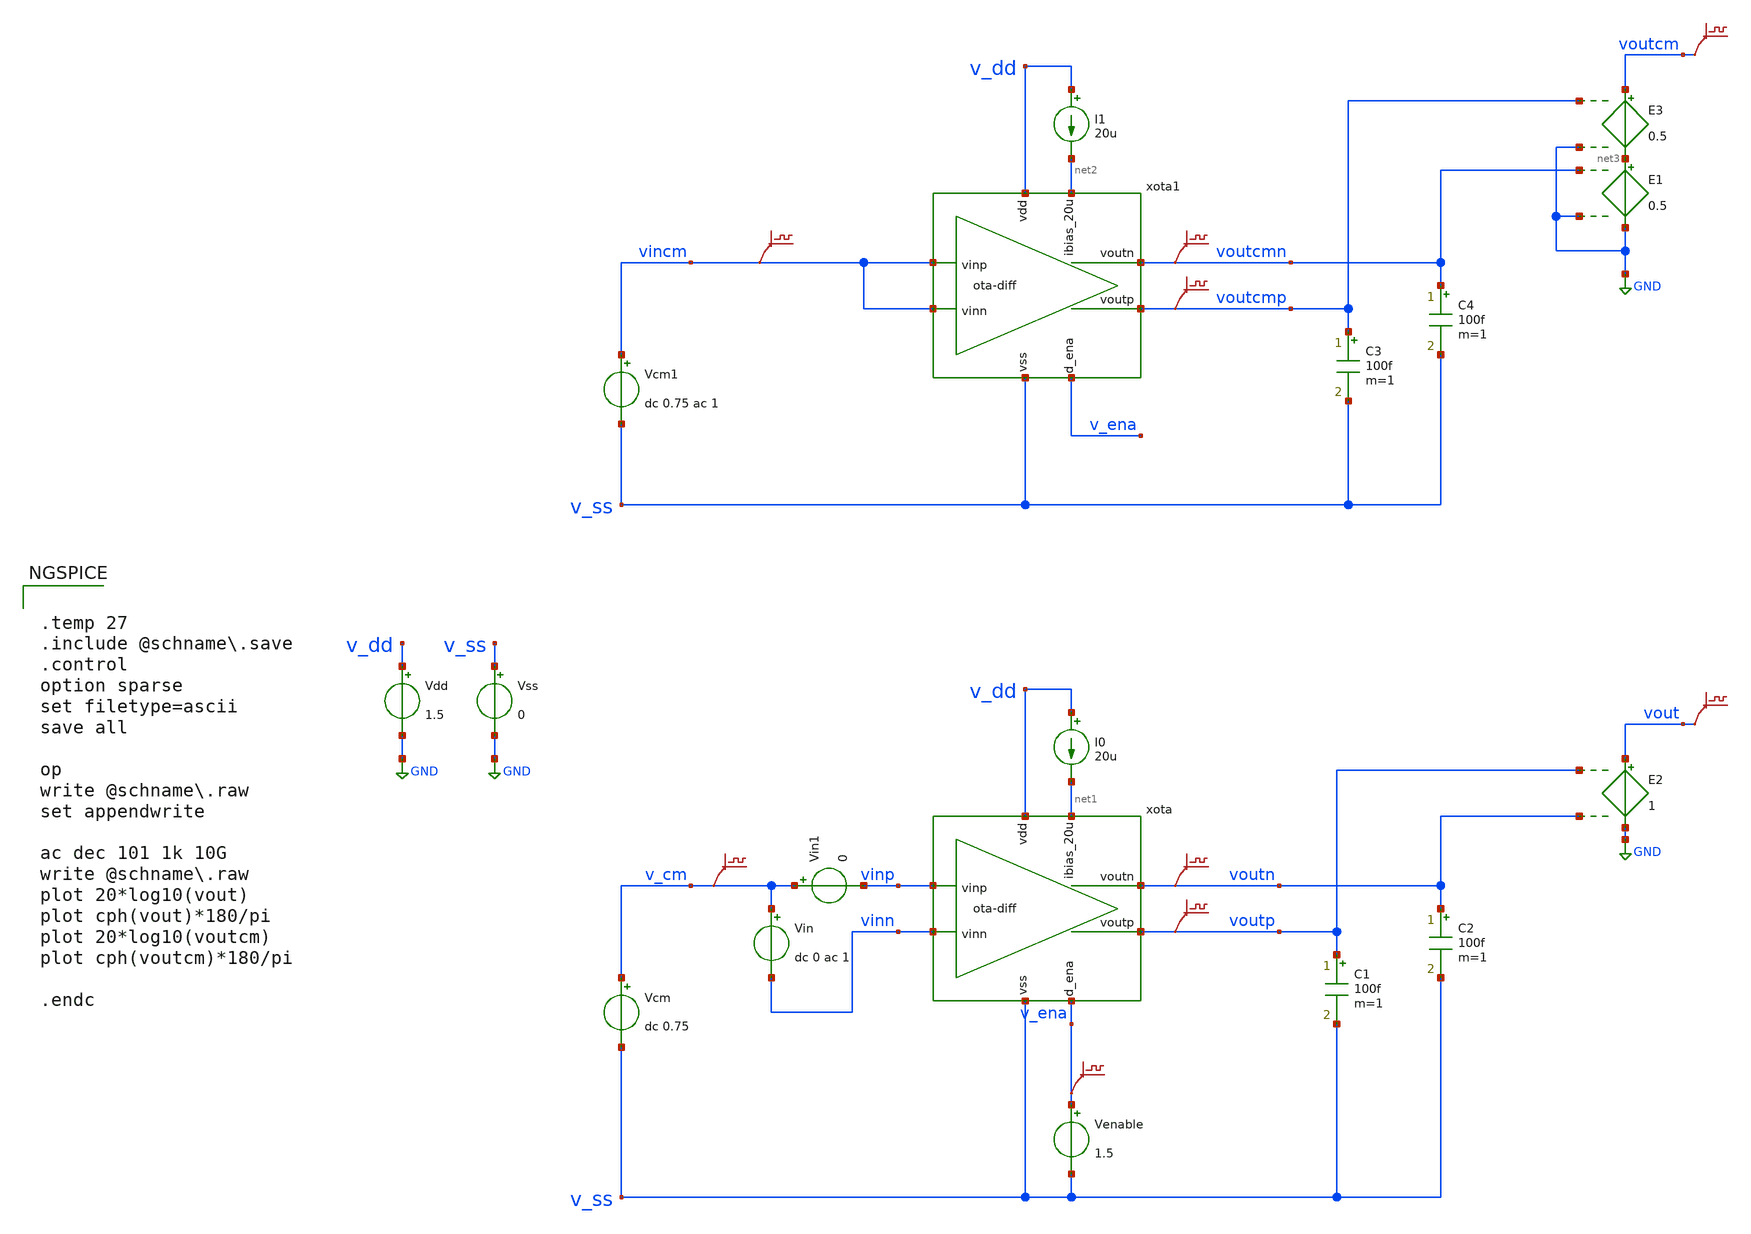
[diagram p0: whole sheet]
** sch_path: xschem/ota-diff_tb-acol.sch
* (c) 2024-2025 Harald Pretl, Apache-2.0 license
**.subckt ota-diff_tb-acol
Vdd v_dd GND 1.5
xota v_dd vinp vinn net1 v_ena v_ss voutn voutp ota-diff
Vss v_ss GND 0
C1 voutp v_ss 100f m=1
Vcm v_cm v_ss dc 0.75
I0 v_dd net1 20u
Venable v_ena v_ss 1.5
.save v(v_cm)
.save v(voutp)
.save v(v_ena)
Vin v_cm vinn dc 0 ac 1
C2 voutn v_ss 100f m=1
.save v(voutn)
xota1 v_dd vincm vincm net2 v_ena v_ss voutcmn voutcmp ota-diff
C3 voutcmp v_ss 100f m=1
Vcm1 vincm v_ss dc 0.75 ac 1
I1 v_dd net2 20u
.save v(vincm)
.save v(voutcmp)
C4 voutcmn v_ss 100f m=1
.save v(voutcmn)
E1 net3 GND voutcmn GND 0.5
.save v(voutcm)
E2 vout GND voutp voutn 1
.save v(vout)
E3 voutcm net3 voutcmp GND 0.5
Vin1 v_cm vinp 0
**** begin user architecture code

.lib cornerMOSlv.lib mos_tt
.lib cornerRES.lib res_typ
.lib cornerCAP.lib cap_typ



.temp 27
.include @schname\.save
.control
option sparse
set filetype=ascii
save all

op
write @schname\.raw
set appendwrite

ac dec 101 1k 10G
write @schname\.raw
plot 20*log10(vout)
plot cph(vout)*180/pi
plot 20*log10(voutcm)
plot cph(voutcm)*180/pi

.endc


**** end user architecture code
**.ends
.GLOBAL GND
.end
